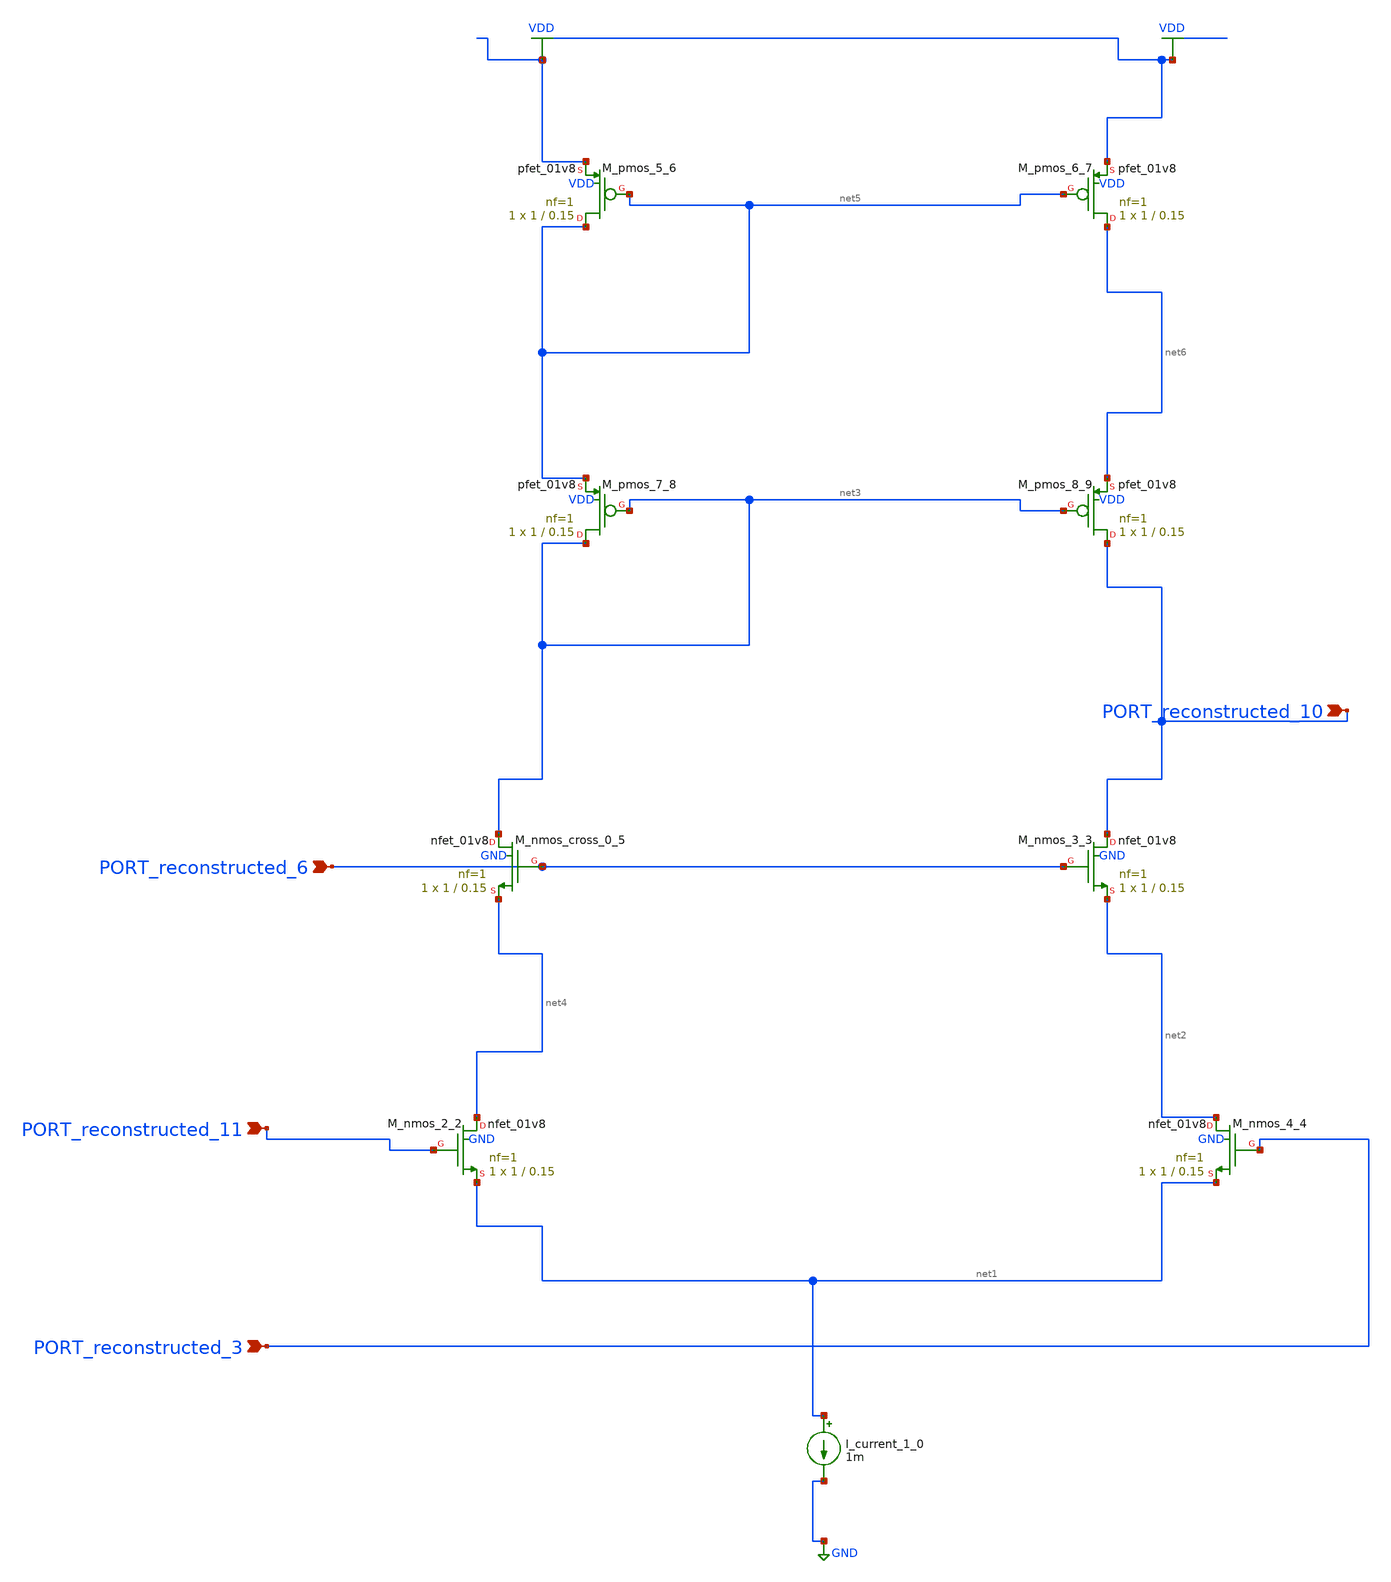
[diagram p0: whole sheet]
** sch_path: schematics/AMSNet/643.sch
**.subckt 643 PORT_reconstructed_11 PORT_reconstructed_6 PORT_reconstructed_10 PORT_reconstructed_3
*.ipin PORT_reconstructed_11
*.ipin PORT_reconstructed_6
*.ipin PORT_reconstructed_10
*.ipin PORT_reconstructed_3
I_current_1_0 net1 GND 1m
XM_nmos_2_2 net4 PORT_reconstructed_11 net1 GND sky130_fd_pr__nfet_01v8 L=0.15 W=1 nf=1 ad='int((1 + 1)/2) * 1 / 1 * 0.29'
+ as='int((1 + 2)/2) * 1 / 1 * 0.29' pd='2*int((1 + 1)/2) * (1 / 1 + 0.29)' ps='2*int((1 + 2)/2) * (1 / 1 + 0.29)'
+ nrd='0.29 / 1 ' nrs='0.29 / 1 ' sa=0 sb=0 sd=0 mult=1 m=1
XM_nmos_3_3 PORT_reconstructed_10 PORT_reconstructed_6 net2 GND sky130_fd_pr__nfet_01v8 L=0.15 W=1 nf=1
+ ad='int((1 + 1)/2) * 1 / 1 * 0.29' as='int((1 + 2)/2) * 1 / 1 * 0.29' pd='2*int((1 + 1)/2) * (1 / 1 + 0.29)'
+ ps='2*int((1 + 2)/2) * (1 / 1 + 0.29)' nrd='0.29 / 1 ' nrs='0.29 / 1 ' sa=0 sb=0 sd=0 mult=1 m=1
XM_nmos_4_4 net2 PORT_reconstructed_3 net1 GND sky130_fd_pr__nfet_01v8 L=0.15 W=1 nf=1 ad='int((1 + 1)/2) * 1 / 1 * 0.29'
+ as='int((1 + 2)/2) * 1 / 1 * 0.29' pd='2*int((1 + 1)/2) * (1 / 1 + 0.29)' ps='2*int((1 + 2)/2) * (1 / 1 + 0.29)'
+ nrd='0.29 / 1 ' nrs='0.29 / 1 ' sa=0 sb=0 sd=0 mult=1 m=1
XM_nmos_cross_0_5 net3 PORT_reconstructed_6 net4 GND sky130_fd_pr__nfet_01v8 L=0.15 W=1 nf=1 ad='int((1 + 1)/2) * 1 / 1 * 0.29'
+ as='int((1 + 2)/2) * 1 / 1 * 0.29' pd='2*int((1 + 1)/2) * (1 / 1 + 0.29)' ps='2*int((1 + 2)/2) * (1 / 1 + 0.29)'
+ nrd='0.29 / 1 ' nrs='0.29 / 1 ' sa=0 sb=0 sd=0 mult=1 m=1
XM_pmos_5_6 net5 net5 VDD VDD sky130_fd_pr__pfet_01v8 L=0.15 W=1 nf=1 ad='int((1 + 1)/2) * 1 / 1 * 0.29'
+ as='int((1 + 2)/2) * 1 / 1 * 0.29' pd='2*int((1 + 1)/2) * (1 / 1 + 0.29)' ps='2*int((1 + 2)/2) * (1 / 1 + 0.29)'
+ nrd='0.29 / 1 ' nrs='0.29 / 1 ' sa=0 sb=0 sd=0 mult=1 m=1
XM_pmos_6_7 net6 net5 VDD VDD sky130_fd_pr__pfet_01v8 L=0.15 W=1 nf=1 ad='int((1 + 1)/2) * 1 / 1 * 0.29'
+ as='int((1 + 2)/2) * 1 / 1 * 0.29' pd='2*int((1 + 1)/2) * (1 / 1 + 0.29)' ps='2*int((1 + 2)/2) * (1 / 1 + 0.29)'
+ nrd='0.29 / 1 ' nrs='0.29 / 1 ' sa=0 sb=0 sd=0 mult=1 m=1
XM_pmos_7_8 net3 net3 net5 VDD sky130_fd_pr__pfet_01v8 L=0.15 W=1 nf=1 ad='int((1 + 1)/2) * 1 / 1 * 0.29'
+ as='int((1 + 2)/2) * 1 / 1 * 0.29' pd='2*int((1 + 1)/2) * (1 / 1 + 0.29)' ps='2*int((1 + 2)/2) * (1 / 1 + 0.29)'
+ nrd='0.29 / 1 ' nrs='0.29 / 1 ' sa=0 sb=0 sd=0 mult=1 m=1
XM_pmos_8_9 PORT_reconstructed_10 net3 net6 VDD sky130_fd_pr__pfet_01v8 L=0.15 W=1 nf=1 ad='int((1 + 1)/2) * 1 / 1 * 0.29'
+ as='int((1 + 2)/2) * 1 / 1 * 0.29' pd='2*int((1 + 1)/2) * (1 / 1 + 0.29)' ps='2*int((1 + 2)/2) * (1 / 1 + 0.29)'
+ nrd='0.29 / 1 ' nrs='0.29 / 1 ' sa=0 sb=0 sd=0 mult=1 m=1
**.ends
.GLOBAL GND
.GLOBAL VDD
.end
